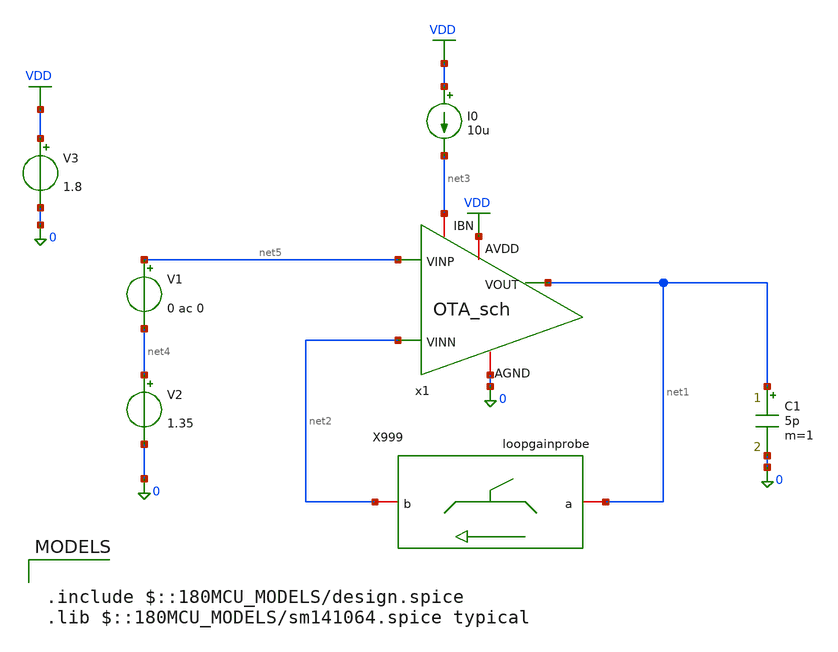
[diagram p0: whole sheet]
** sch_path: Lab_07/OTA_CL.sch
**.subckt OTA_CL
x1 net5 VDD net2 net3 0 net1 OTA_sch
X999 net1 net2 loopgainprobe
C1 net1 0 5p m=1
V3 VDD 0 1.8
I0 VDD net3 10u
V1 net5 net4 0 ac 0
V2 net4 0 1.35
**** begin user architecture code

.include $::180MCU_MODELS/design.spice
.lib $::180MCU_MODELS/sm141064.spice typical



.include /home/ubuntu/LoopGainProbe/stb.spi


**** end user architecture code
**.ends
.GLOBAL VDD
.end
